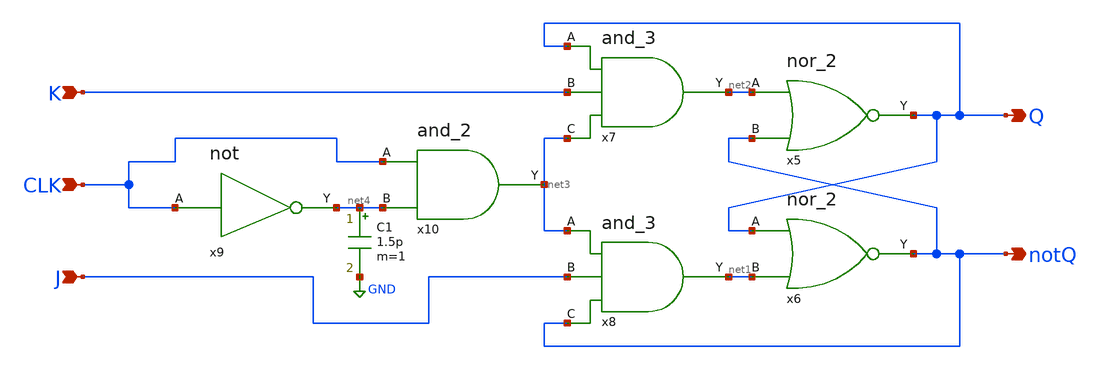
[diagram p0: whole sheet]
** sch_path: Circuiti/latches_sch_sym/jk_flip_flop.sch
**.subckt jk_flip_flop K J Q notQ CLK
*.ipin K
*.ipin J
*.opin Q
*.opin notQ
*.ipin CLK
x5 net2 Q notQ nor_2
x6 Q notQ net1 nor_2
x7 Q net2 K net3 and_3
x8 net3 net1 J notQ and_3
x9 CLK net4 not
x10 CLK net3 net4 and_2
C1 net4 GND 1.5p m=1
**.ends

* expanding   symbol:  /home/matteo/Documenti/tesi/Circuiti/logic_gates_sch_sym/nor_2.sym # of
*+ pins=3
** sym_path: Circuiti/logic_gates_sch_sym/nor_2.sym
** sch_path: Circuiti/logic_gates_sch_sym/nor_2.sch
.subckt nor_2 A Y B
*.opin Y
*.ipin A
*.ipin B
XM1 Y B GND GND sky130_fd_pr__nfet_01v8 L=0.45 W=1 nf=1 ad='int((nf+1)/2) * W/nf * 0.29' as='int((nf+2)/2) * W/nf * 0.29'
+ pd='2*int((nf+1)/2) * (W/nf + 0.29)' ps='2*int((nf+2)/2) * (W/nf + 0.29)' nrd='0.29 / W' nrs='0.29 / W'
+ sa=0 sb=0 sd=0 mult=1 m=1
XM3 Y B net1 VDD sky130_fd_pr__pfet_01v8 L=0.15 W=4.8 nf=1 ad='int((nf+1)/2) * W/nf * 0.29' as='int((nf+2)/2) * W/nf * 0.29'
+ pd='2*int((nf+1)/2) * (W/nf + 0.29)' ps='2*int((nf+2)/2) * (W/nf + 0.29)' nrd='0.29 / W' nrs='0.29 / W'
+ sa=0 sb=0 sd=0 mult=1 m=1
XM4 net1 A Vdd VDD sky130_fd_pr__pfet_01v8 L=0.15 W=4.8 nf=1 ad='int((nf+1)/2) * W/nf * 0.29' as='int((nf+2)/2) * W/nf * 0.29'
+ pd='2*int((nf+1)/2) * (W/nf + 0.29)' ps='2*int((nf+2)/2) * (W/nf + 0.29)' nrd='0.29 / W' nrs='0.29 / W'
+ sa=0 sb=0 sd=0 mult=1 m=1
XM2 Y A GND GND sky130_fd_pr__nfet_01v8 L=0.45 W=1 nf=1 ad='int((nf+1)/2) * W/nf * 0.29' as='int((nf+2)/2) * W/nf * 0.29'
+ pd='2*int((nf+1)/2) * (W/nf + 0.29)' ps='2*int((nf+2)/2) * (W/nf + 0.29)' nrd='0.29 / W' nrs='0.29 / W'
+ sa=0 sb=0 sd=0 mult=1 m=1
.ends


* expanding   symbol:  /home/matteo/Documenti/tesi/Circuiti/logic_gates_sch_sym/and_3.sym # of
*+ pins=4
** sym_path: Circuiti/logic_gates_sch_sym/and_3.sym
** sch_path: Circuiti/logic_gates_sch_sym/and_3.sch
.subckt and_3 A Y B C
*.ipin A
*.ipin B
*.ipin C
*.opin Y
x1 A Y net1 and_2
x2 B net1 C and_2
.ends


* expanding   symbol:  /home/matteo/Documenti/tesi/Circuiti/logic_gates_sch_sym/not.sym # of pins=2
** sym_path: Circuiti/logic_gates_sch_sym/not.sym
** sch_path: Circuiti/logic_gates_sch_sym/not.sch
.subckt not A Y
*.ipin A
*.opin Y
XM1 Y A GND GND sky130_fd_pr__nfet_01v8 L=0.45 W=1 nf=1 ad='int((nf+1)/2) * W/nf * 0.29' as='int((nf+2)/2) * W/nf * 0.29'
+ pd='2*int((nf+1)/2) * (W/nf + 0.29)' ps='2*int((nf+2)/2) * (W/nf + 0.29)' nrd='0.29 / W' nrs='0.29 / W'
+ sa=0 sb=0 sd=0 mult=1 m=1
XM2 Y A Vdd VDD sky130_fd_pr__pfet_01v8 L=0.45 W=4.8 nf=1 ad='int((nf+1)/2) * W/nf * 0.29' as='int((nf+2)/2) * W/nf * 0.29'
+ pd='2*int((nf+1)/2) * (W/nf + 0.29)' ps='2*int((nf+2)/2) * (W/nf + 0.29)' nrd='0.29 / W' nrs='0.29 / W'
+ sa=0 sb=0 sd=0 mult=1 m=1
.ends


* expanding   symbol:  /home/matteo/Documenti/tesi/Circuiti/logic_gates_sch_sym/and_2.sym # of
*+ pins=3
** sym_path: Circuiti/logic_gates_sch_sym/and_2.sym
** sch_path: Circuiti/logic_gates_sch_sym/and_2.sch
.subckt and_2 A Y B
*.ipin B
*.ipin A
*.opin Y
x1 A net1 B nand_2
x2 net1 Y not
.ends


* expanding   symbol:  /home/matteo/Documenti/tesi/Circuiti/logic_gates_sch_sym/nand_2.sym # of
*+ pins=3
** sym_path: Circuiti/logic_gates_sch_sym/nand_2.sym
** sch_path: Circuiti/logic_gates_sch_sym/nand_2.sch
.subckt nand_2 A Y B
*.ipin A
*.ipin B
*.opin Y
XM1 Y A net1 GND sky130_fd_pr__nfet_01v8 L=0.15 W=1 nf=1 ad='int((nf+1)/2) * W/nf * 0.29' as='int((nf+2)/2) * W/nf * 0.29'
+ pd='2*int((nf+1)/2) * (W/nf + 0.29)' ps='2*int((nf+2)/2) * (W/nf + 0.29)' nrd='0.29 / W' nrs='0.29 / W'
+ sa=0 sb=0 sd=0 mult=1 m=1
XM3 Y B Vdd VDD sky130_fd_pr__pfet_01v8 L=0.45 W=4.8 nf=1 ad='int((nf+1)/2) * W/nf * 0.29' as='int((nf+2)/2) * W/nf * 0.29'
+ pd='2*int((nf+1)/2) * (W/nf + 0.29)' ps='2*int((nf+2)/2) * (W/nf + 0.29)' nrd='0.29 / W' nrs='0.29 / W'
+ sa=0 sb=0 sd=0 mult=1 m=1
XM4 Y A Vdd VDD sky130_fd_pr__pfet_01v8 L=0.45 W=4.8 nf=1 ad='int((nf+1)/2) * W/nf * 0.29' as='int((nf+2)/2) * W/nf * 0.29'
+ pd='2*int((nf+1)/2) * (W/nf + 0.29)' ps='2*int((nf+2)/2) * (W/nf + 0.29)' nrd='0.29 / W' nrs='0.29 / W'
+ sa=0 sb=0 sd=0 mult=1 m=1
XM2 net1 B GND GND sky130_fd_pr__nfet_01v8 L=0.15 W=1 nf=1 ad='int((nf+1)/2) * W/nf * 0.29' as='int((nf+2)/2) * W/nf * 0.29'
+ pd='2*int((nf+1)/2) * (W/nf + 0.29)' ps='2*int((nf+2)/2) * (W/nf + 0.29)' nrd='0.29 / W' nrs='0.29 / W'
+ sa=0 sb=0 sd=0 mult=1 m=1
.ends

.GLOBAL GND
.GLOBAL Vdd
.end
